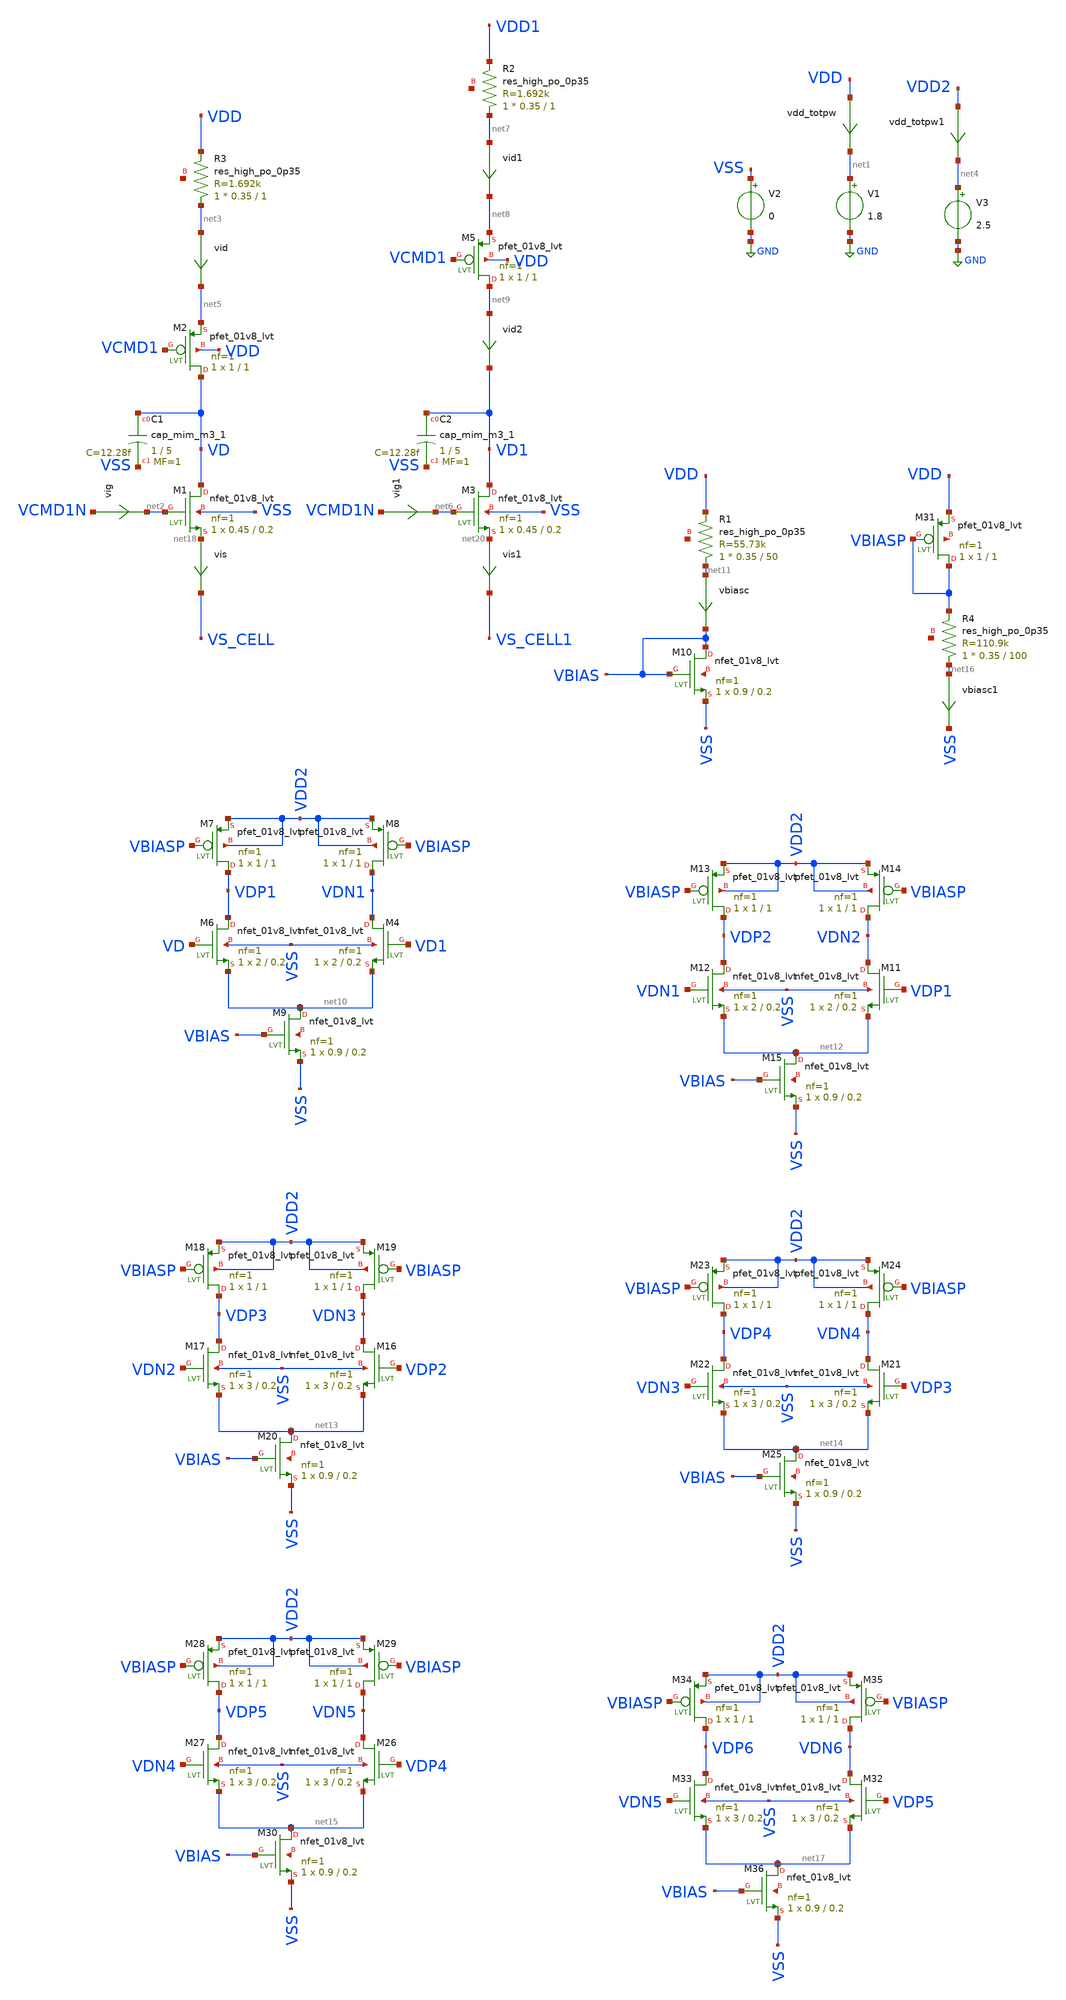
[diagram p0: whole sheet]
** sch_path: xschem/tb_em_dram_cell_sourcecap2.sch
**.subckt tb_em_dram_cell_sourcecap2
V1 net1 GND 1.8
V2 VSS GND 0
vdd_totpw VDD net1 0
.save i(vdd_totpw)
vis net18 VS_CELL 0
.save i(vis)
XR3 net3 VDD net19 sky130_fd_pr__res_high_po_0p35 L=1 mult=1 m=1
vig VCMD1N net2 0
.save i(vig)
vid net3 net5 0
.save i(vid)
XC1 VD VSS sky130_fd_pr__cap_mim_m3_1 W=1 L=5 MF=1 m=1
V3 net4 GND 2.5
vdd_totpw1 VDD2 net4 0
.save i(vdd_totpw1)
XM2 VD VCMD1 net5 VDD sky130_fd_pr__pfet_01v8_lvt L=1 W=1 nf=1 ad='int((nf+1)/2) * W/nf * 0.29' as='int((nf+2)/2) * W/nf * 0.29'
+ pd='2*int((nf+1)/2) * (W/nf + 0.29)' ps='2*int((nf+2)/2) * (W/nf + 0.29)' nrd='0.29 / W' nrs='0.29 / W'
+ sa=0 sb=0 sd=0 mult=1 m=1
vis1 net20 VS_CELL1 0
.save i(vis1)
XR2 net7 VDD1 net21 sky130_fd_pr__res_high_po_0p35 L=1 mult=1 m=1
vig1 VCMD1N net6 0
.save i(vig1)
vid1 net7 net8 0
.save i(vid1)
XC2 VD1 VSS sky130_fd_pr__cap_mim_m3_1 W=1 L=5 MF=1 m=1
XM5 net9 VCMD1 net8 VDD sky130_fd_pr__pfet_01v8_lvt L=1 W=1 nf=1 ad='int((nf+1)/2) * W/nf * 0.29' as='int((nf+2)/2) * W/nf * 0.29'
+ pd='2*int((nf+1)/2) * (W/nf + 0.29)' ps='2*int((nf+2)/2) * (W/nf + 0.29)' nrd='0.29 / W' nrs='0.29 / W'
+ sa=0 sb=0 sd=0 mult=1 m=1
vid2 net9 VD1 0
.save i(vid2)
XM1 VD net2 net18 VSS sky130_fd_pr__nfet_01v8_lvt L=0.2 W=0.45 nf=1 ad=0.4 as=0.4 pd='2*int((nf+1)/2) * (W/nf + 0.29)'
+ ps='2*int((nf+2)/2) * (W/nf + 0.29)' nrd='0.29 / W' nrs='0.29 / W' sa=0 sb=0 sd=0 mult=1 m=1
XM3 VD1 net6 net20 VSS sky130_fd_pr__nfet_01v8_lvt L=0.2 W=0.45 nf=1 ad=0.4 as=0.4 pd='2*int((nf+1)/2) * (W/nf + 0.29)'
+ ps='2*int((nf+2)/2) * (W/nf + 0.29)' nrd='0.29 / W' nrs='0.29 / W' sa=0 sb=0 sd=0 mult=1 m=1
XM4 VDN1 VD1 net10 VSS sky130_fd_pr__nfet_01v8_lvt L=0.2 W=2 nf=1 ad=0.4 as=0.4 pd='2*int((nf+1)/2) * (W/nf + 0.29)'
+ ps='2*int((nf+2)/2) * (W/nf + 0.29)' nrd='0.29 / W' nrs='0.29 / W' sa=0 sb=0 sd=0 mult=1 m=1
XM6 VDP1 VD net10 VSS sky130_fd_pr__nfet_01v8_lvt L=0.2 W=2 nf=1 ad=0.4 as=0.4 pd='2*int((nf+1)/2) * (W/nf + 0.29)'
+ ps='2*int((nf+2)/2) * (W/nf + 0.29)' nrd='0.29 / W' nrs='0.29 / W' sa=0 sb=0 sd=0 mult=1 m=1
XM7 VDP1 VBIASP VDD2 VDD2 sky130_fd_pr__pfet_01v8_lvt L=1 W=1 nf=1 ad='int((nf+1)/2) * W/nf * 0.29' as='int((nf+2)/2) * W/nf * 0.29'
+ pd='2*int((nf+1)/2) * (W/nf + 0.29)' ps='2*int((nf+2)/2) * (W/nf + 0.29)' nrd='0.29 / W' nrs='0.29 / W'
+ sa=0 sb=0 sd=0 mult=1 m=1
XM8 VDN1 VBIASP VDD2 VDD2 sky130_fd_pr__pfet_01v8_lvt L=1 W=1 nf=1 ad='int((nf+1)/2) * W/nf * 0.29' as='int((nf+2)/2) * W/nf * 0.29'
+ pd='2*int((nf+1)/2) * (W/nf + 0.29)' ps='2*int((nf+2)/2) * (W/nf + 0.29)' nrd='0.29 / W' nrs='0.29 / W'
+ sa=0 sb=0 sd=0 mult=1 m=1
XM9 net10 VBIAS VSS net22 sky130_fd_pr__nfet_01v8_lvt L=0.2 W=0.9 nf=1 ad=0.4 as=0.4 pd='2*int((nf+1)/2) * (W/nf + 0.29)'
+ ps='2*int((nf+2)/2) * (W/nf + 0.29)' nrd='0.29 / W' nrs='0.29 / W' sa=0 sb=0 sd=0 mult=1 m=1
XM10 VBIAS VBIAS VSS net23 sky130_fd_pr__nfet_01v8_lvt L=0.2 W=0.9 nf=1 ad=0.4 as=0.4 pd='2*int((nf+1)/2) * (W/nf + 0.29)'
+ ps='2*int((nf+2)/2) * (W/nf + 0.29)' nrd='0.29 / W' nrs='0.29 / W' sa=0 sb=0 sd=0 mult=1 m=1
XR1 net11 VDD net24 sky130_fd_pr__res_high_po_0p35 L=50 mult=1 m=1
vbiasc net11 VBIAS 0
.save i(vbiasc)
XM11 VDN2 VDP1 net12 VSS sky130_fd_pr__nfet_01v8_lvt L=0.2 W=2 nf=1 ad=0.4 as=0.4 pd='2*int((nf+1)/2) * (W/nf + 0.29)'
+ ps='2*int((nf+2)/2) * (W/nf + 0.29)' nrd='0.29 / W' nrs='0.29 / W' sa=0 sb=0 sd=0 mult=1 m=1
XM12 VDP2 VDN1 net12 VSS sky130_fd_pr__nfet_01v8_lvt L=0.2 W=2 nf=1 ad=0.4 as=0.4 pd='2*int((nf+1)/2) * (W/nf + 0.29)'
+ ps='2*int((nf+2)/2) * (W/nf + 0.29)' nrd='0.29 / W' nrs='0.29 / W' sa=0 sb=0 sd=0 mult=1 m=1
XM13 VDP2 VBIASP VDD2 VDD2 sky130_fd_pr__pfet_01v8_lvt L=1 W=1 nf=1 ad='int((nf+1)/2) * W/nf * 0.29'
+ as='int((nf+2)/2) * W/nf * 0.29' pd='2*int((nf+1)/2) * (W/nf + 0.29)' ps='2*int((nf+2)/2) * (W/nf + 0.29)'
+ nrd='0.29 / W' nrs='0.29 / W' sa=0 sb=0 sd=0 mult=1 m=1
XM14 VDN2 VBIASP VDD2 VDD2 sky130_fd_pr__pfet_01v8_lvt L=1 W=1 nf=1 ad='int((nf+1)/2) * W/nf * 0.29'
+ as='int((nf+2)/2) * W/nf * 0.29' pd='2*int((nf+1)/2) * (W/nf + 0.29)' ps='2*int((nf+2)/2) * (W/nf + 0.29)'
+ nrd='0.29 / W' nrs='0.29 / W' sa=0 sb=0 sd=0 mult=1 m=1
XM15 net12 VBIAS VSS net25 sky130_fd_pr__nfet_01v8_lvt L=0.2 W=0.9 nf=1 ad=0.4 as=0.4 pd='2*int((nf+1)/2) * (W/nf + 0.29)'
+ ps='2*int((nf+2)/2) * (W/nf + 0.29)' nrd='0.29 / W' nrs='0.29 / W' sa=0 sb=0 sd=0 mult=1 m=1
XM16 VDN3 VDP2 net13 VSS sky130_fd_pr__nfet_01v8_lvt L=0.2 W=3 nf=1 ad=0.4 as=0.4 pd='2*int((nf+1)/2) * (W/nf + 0.29)'
+ ps='2*int((nf+2)/2) * (W/nf + 0.29)' nrd='0.29 / W' nrs='0.29 / W' sa=0 sb=0 sd=0 mult=1 m=1
XM17 VDP3 VDN2 net13 VSS sky130_fd_pr__nfet_01v8_lvt L=0.2 W=3 nf=1 ad=0.4 as=0.4 pd='2*int((nf+1)/2) * (W/nf + 0.29)'
+ ps='2*int((nf+2)/2) * (W/nf + 0.29)' nrd='0.29 / W' nrs='0.29 / W' sa=0 sb=0 sd=0 mult=1 m=1
XM18 VDP3 VBIASP VDD2 VDD2 sky130_fd_pr__pfet_01v8_lvt L=1 W=1 nf=1 ad='int((nf+1)/2) * W/nf * 0.29'
+ as='int((nf+2)/2) * W/nf * 0.29' pd='2*int((nf+1)/2) * (W/nf + 0.29)' ps='2*int((nf+2)/2) * (W/nf + 0.29)'
+ nrd='0.29 / W' nrs='0.29 / W' sa=0 sb=0 sd=0 mult=1 m=1
XM19 VDN3 VBIASP VDD2 VDD2 sky130_fd_pr__pfet_01v8_lvt L=1 W=1 nf=1 ad='int((nf+1)/2) * W/nf * 0.29'
+ as='int((nf+2)/2) * W/nf * 0.29' pd='2*int((nf+1)/2) * (W/nf + 0.29)' ps='2*int((nf+2)/2) * (W/nf + 0.29)'
+ nrd='0.29 / W' nrs='0.29 / W' sa=0 sb=0 sd=0 mult=1 m=1
XM20 net13 VBIAS VSS net26 sky130_fd_pr__nfet_01v8_lvt L=0.2 W=0.9 nf=1 ad=0.4 as=0.4 pd='2*int((nf+1)/2) * (W/nf + 0.29)'
+ ps='2*int((nf+2)/2) * (W/nf + 0.29)' nrd='0.29 / W' nrs='0.29 / W' sa=0 sb=0 sd=0 mult=1 m=1
XM21 VDN4 VDP3 net14 VSS sky130_fd_pr__nfet_01v8_lvt L=0.2 W=3 nf=1 ad=0.4 as=0.4 pd='2*int((nf+1)/2) * (W/nf + 0.29)'
+ ps='2*int((nf+2)/2) * (W/nf + 0.29)' nrd='0.29 / W' nrs='0.29 / W' sa=0 sb=0 sd=0 mult=1 m=1
XM22 VDP4 VDN3 net14 VSS sky130_fd_pr__nfet_01v8_lvt L=0.2 W=3 nf=1 ad=0.4 as=0.4 pd='2*int((nf+1)/2) * (W/nf + 0.29)'
+ ps='2*int((nf+2)/2) * (W/nf + 0.29)' nrd='0.29 / W' nrs='0.29 / W' sa=0 sb=0 sd=0 mult=1 m=1
XM23 VDP4 VBIASP VDD2 VDD2 sky130_fd_pr__pfet_01v8_lvt L=1 W=1 nf=1 ad='int((nf+1)/2) * W/nf * 0.29'
+ as='int((nf+2)/2) * W/nf * 0.29' pd='2*int((nf+1)/2) * (W/nf + 0.29)' ps='2*int((nf+2)/2) * (W/nf + 0.29)'
+ nrd='0.29 / W' nrs='0.29 / W' sa=0 sb=0 sd=0 mult=1 m=1
XM24 VDN4 VBIASP VDD2 VDD2 sky130_fd_pr__pfet_01v8_lvt L=1 W=1 nf=1 ad='int((nf+1)/2) * W/nf * 0.29'
+ as='int((nf+2)/2) * W/nf * 0.29' pd='2*int((nf+1)/2) * (W/nf + 0.29)' ps='2*int((nf+2)/2) * (W/nf + 0.29)'
+ nrd='0.29 / W' nrs='0.29 / W' sa=0 sb=0 sd=0 mult=1 m=1
XM25 net14 VBIAS VSS net27 sky130_fd_pr__nfet_01v8_lvt L=0.2 W=0.9 nf=1 ad=0.4 as=0.4 pd='2*int((nf+1)/2) * (W/nf + 0.29)'
+ ps='2*int((nf+2)/2) * (W/nf + 0.29)' nrd='0.29 / W' nrs='0.29 / W' sa=0 sb=0 sd=0 mult=1 m=1
XM26 VDN5 VDP4 net15 VSS sky130_fd_pr__nfet_01v8_lvt L=0.2 W=3 nf=1 ad=0.4 as=0.4 pd='2*int((nf+1)/2) * (W/nf + 0.29)'
+ ps='2*int((nf+2)/2) * (W/nf + 0.29)' nrd='0.29 / W' nrs='0.29 / W' sa=0 sb=0 sd=0 mult=1 m=1
XM27 VDP5 VDN4 net15 VSS sky130_fd_pr__nfet_01v8_lvt L=0.2 W=3 nf=1 ad=0.4 as=0.4 pd='2*int((nf+1)/2) * (W/nf + 0.29)'
+ ps='2*int((nf+2)/2) * (W/nf + 0.29)' nrd='0.29 / W' nrs='0.29 / W' sa=0 sb=0 sd=0 mult=1 m=1
XM28 VDP5 VBIASP VDD2 VDD2 sky130_fd_pr__pfet_01v8_lvt L=1 W=1 nf=1 ad='int((nf+1)/2) * W/nf * 0.29'
+ as='int((nf+2)/2) * W/nf * 0.29' pd='2*int((nf+1)/2) * (W/nf + 0.29)' ps='2*int((nf+2)/2) * (W/nf + 0.29)'
+ nrd='0.29 / W' nrs='0.29 / W' sa=0 sb=0 sd=0 mult=1 m=1
XM29 VDN5 VBIASP VDD2 VDD2 sky130_fd_pr__pfet_01v8_lvt L=1 W=1 nf=1 ad='int((nf+1)/2) * W/nf * 0.29'
+ as='int((nf+2)/2) * W/nf * 0.29' pd='2*int((nf+1)/2) * (W/nf + 0.29)' ps='2*int((nf+2)/2) * (W/nf + 0.29)'
+ nrd='0.29 / W' nrs='0.29 / W' sa=0 sb=0 sd=0 mult=1 m=1
XM30 net15 VBIAS VSS net28 sky130_fd_pr__nfet_01v8_lvt L=0.2 W=0.9 nf=1 ad=0.4 as=0.4 pd='2*int((nf+1)/2) * (W/nf + 0.29)'
+ ps='2*int((nf+2)/2) * (W/nf + 0.29)' nrd='0.29 / W' nrs='0.29 / W' sa=0 sb=0 sd=0 mult=1 m=1
XR4 net16 VBIASP net29 sky130_fd_pr__res_high_po_0p35 L=100 mult=1 m=1
vbiasc1 net16 VSS 0
.save i(vbiasc1)
XM31 VBIASP VBIASP VDD net30 sky130_fd_pr__pfet_01v8_lvt L=1 W=1 nf=1 ad='int((nf+1)/2) * W/nf * 0.29'
+ as='int((nf+2)/2) * W/nf * 0.29' pd='2*int((nf+1)/2) * (W/nf + 0.29)' ps='2*int((nf+2)/2) * (W/nf + 0.29)'
+ nrd='0.29 / W' nrs='0.29 / W' sa=0 sb=0 sd=0 mult=1 m=1
XM32 VDN6 VDP5 net17 VSS sky130_fd_pr__nfet_01v8_lvt L=0.2 W=3 nf=1 ad=0.4 as=0.4 pd='2*int((nf+1)/2) * (W/nf + 0.29)'
+ ps='2*int((nf+2)/2) * (W/nf + 0.29)' nrd='0.29 / W' nrs='0.29 / W' sa=0 sb=0 sd=0 mult=1 m=1
XM33 VDP6 VDN5 net17 VSS sky130_fd_pr__nfet_01v8_lvt L=0.2 W=3 nf=1 ad=0.4 as=0.4 pd='2*int((nf+1)/2) * (W/nf + 0.29)'
+ ps='2*int((nf+2)/2) * (W/nf + 0.29)' nrd='0.29 / W' nrs='0.29 / W' sa=0 sb=0 sd=0 mult=1 m=1
XM34 VDP6 VBIASP VDD2 VDD2 sky130_fd_pr__pfet_01v8_lvt L=1 W=1 nf=1 ad='int((nf+1)/2) * W/nf * 0.29'
+ as='int((nf+2)/2) * W/nf * 0.29' pd='2*int((nf+1)/2) * (W/nf + 0.29)' ps='2*int((nf+2)/2) * (W/nf + 0.29)'
+ nrd='0.29 / W' nrs='0.29 / W' sa=0 sb=0 sd=0 mult=1 m=1
XM35 VDN6 VBIASP VDD2 VDD2 sky130_fd_pr__pfet_01v8_lvt L=1 W=1 nf=1 ad='int((nf+1)/2) * W/nf * 0.29'
+ as='int((nf+2)/2) * W/nf * 0.29' pd='2*int((nf+1)/2) * (W/nf + 0.29)' ps='2*int((nf+2)/2) * (W/nf + 0.29)'
+ nrd='0.29 / W' nrs='0.29 / W' sa=0 sb=0 sd=0 mult=1 m=1
XM36 net17 VBIAS VSS net31 sky130_fd_pr__nfet_01v8_lvt L=0.2 W=0.9 nf=1 ad=0.4 as=0.4 pd='2*int((nf+1)/2) * (W/nf + 0.29)'
+ ps='2*int((nf+2)/2) * (W/nf + 0.29)' nrd='0.29 / W' nrs='0.29 / W' sa=0 sb=0 sd=0 mult=1 m=1
**** begin user architecture code

** opencircuitdesign pdks install
.lib $::SKYWATER_MODELS/sky130.lib.spice tt
*.lib $::SKYWATER_STDCELLS/sky130_fd_sc_hd_blablabla.spice

.subckt sky130_fd_sc_hd__inv_1 A VGND VNB VPB VPWR Y
X0 VGND A Y VNB sky130_fd_pr__nfet_01v8 w=650000u l=150000u
X1 VPWR A Y VPB sky130_fd_pr__pfet_01v8_hvt w=1e+06u l=150000u
.ends





.options savecurrents
VCMD2 VCMD2   0 sine  0.9 0.9  10k 0 0
VCMD1N VCMD1N 0 pulse 0   1.8 0.4u 1n 1n 50n  1u
VCMD1 VCMD1   0 pulse 1.8 0   0.3u 1n 1n 0.4u 10u
VDD1 VDD1     0 pulse 1.8 0   0.2u 1n 1n 0.4u 6u
.control
  repeat 3
    save all
    tran 0.1n 2u
    remzerovec
    write tb_em_dram_cell_sourcecap2.raw
    set appendwrite
    reset
    end
.endc



**** end user architecture code
**.ends
.GLOBAL GND
.end
